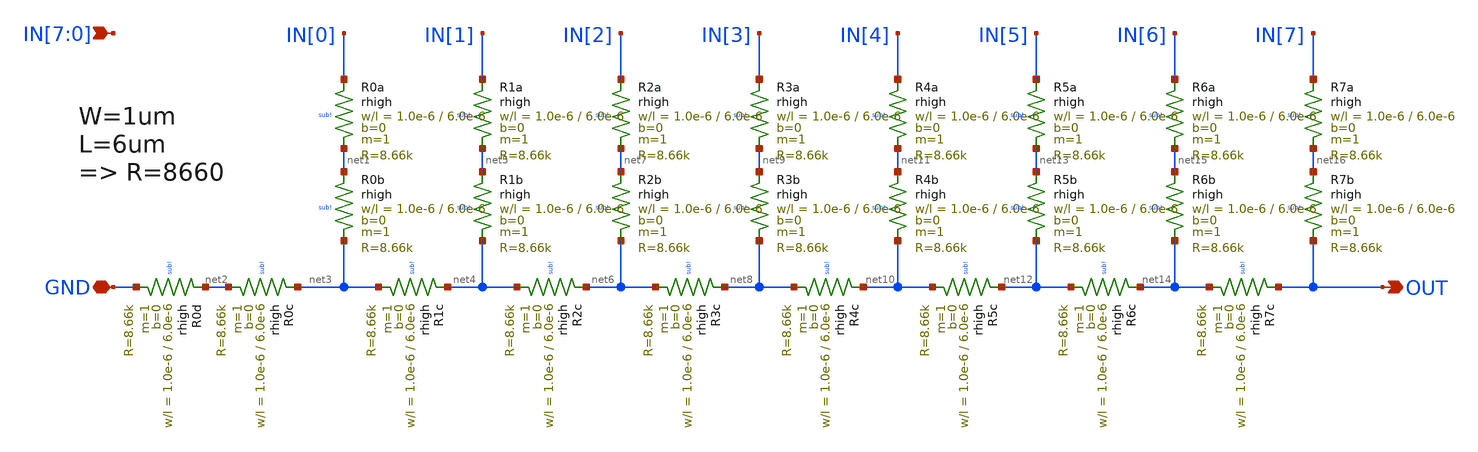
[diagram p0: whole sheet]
** sch_path: xschem/r2r_dac.sch
**.subckt r2r_dac IN[7],IN[6],IN[5],IN[4],IN[3],IN[2],IN[1],IN[0] GND OUT
*.ipin IN[7],IN[6],IN[5],IN[4],IN[3],IN[2],IN[1],IN[0]
*.iopin GND
*.opin OUT
XR0a IN[0] net1 sub! rhigh w=1.0e-6 l=6.0e-6 m=1 b=0 mm_ok=1
XR0b net1 net3 sub! rhigh w=1.0e-6 l=6.0e-6 m=1 b=0 mm_ok=1
XR1c net4 net3 sub! rhigh w=1.0e-6 l=6.0e-6 m=1 b=0 mm_ok=1
XR0c net3 net2 sub! rhigh w=1.0e-6 l=6.0e-6 m=1 b=0 mm_ok=1
XR0d net2 GND sub! rhigh w=1.0e-6 l=6.0e-6 m=1 b=0 mm_ok=1
XR1a IN[1] net5 sub! rhigh w=1.0e-6 l=6.0e-6 m=1 b=0 mm_ok=1
XR1b net5 net4 sub! rhigh w=1.0e-6 l=6.0e-6 m=1 b=0 mm_ok=1
XR2c net6 net4 sub! rhigh w=1.0e-6 l=6.0e-6 m=1 b=0 mm_ok=1
XR2a IN[2] net7 sub! rhigh w=1.0e-6 l=6.0e-6 m=1 b=0 mm_ok=1
XR2b net7 net6 sub! rhigh w=1.0e-6 l=6.0e-6 m=1 b=0 mm_ok=1
XR3c net8 net6 sub! rhigh w=1.0e-6 l=6.0e-6 m=1 b=0 mm_ok=1
XR3a IN[3] net9 sub! rhigh w=1.0e-6 l=6.0e-6 m=1 b=0 mm_ok=1
XR3b net9 net8 sub! rhigh w=1.0e-6 l=6.0e-6 m=1 b=0 mm_ok=1
XR4c net10 net8 sub! rhigh w=1.0e-6 l=6.0e-6 m=1 b=0 mm_ok=1
XR4a IN[4] net11 sub! rhigh w=1.0e-6 l=6.0e-6 m=1 b=0 mm_ok=1
XR4b net11 net10 sub! rhigh w=1.0e-6 l=6.0e-6 m=1 b=0 mm_ok=1
XR5c net12 net10 sub! rhigh w=1.0e-6 l=6.0e-6 m=1 b=0 mm_ok=1
XR5a IN[5] net13 sub! rhigh w=1.0e-6 l=6.0e-6 m=1 b=0 mm_ok=1
XR5b net13 net12 sub! rhigh w=1.0e-6 l=6.0e-6 m=1 b=0 mm_ok=1
XR6c net14 net12 sub! rhigh w=1.0e-6 l=6.0e-6 m=1 b=0 mm_ok=1
XR6a IN[6] net15 sub! rhigh w=1.0e-6 l=6.0e-6 m=1 b=0 mm_ok=1
XR6b net15 net14 sub! rhigh w=1.0e-6 l=6.0e-6 m=1 b=0 mm_ok=1
XR7c OUT net14 sub! rhigh w=1.0e-6 l=6.0e-6 m=1 b=0 mm_ok=1
XR7a IN[7] net16 sub! rhigh w=1.0e-6 l=6.0e-6 m=1 b=0 mm_ok=1
XR7b net16 OUT sub! rhigh w=1.0e-6 l=6.0e-6 m=1 b=0 mm_ok=1
**.ends
.end
